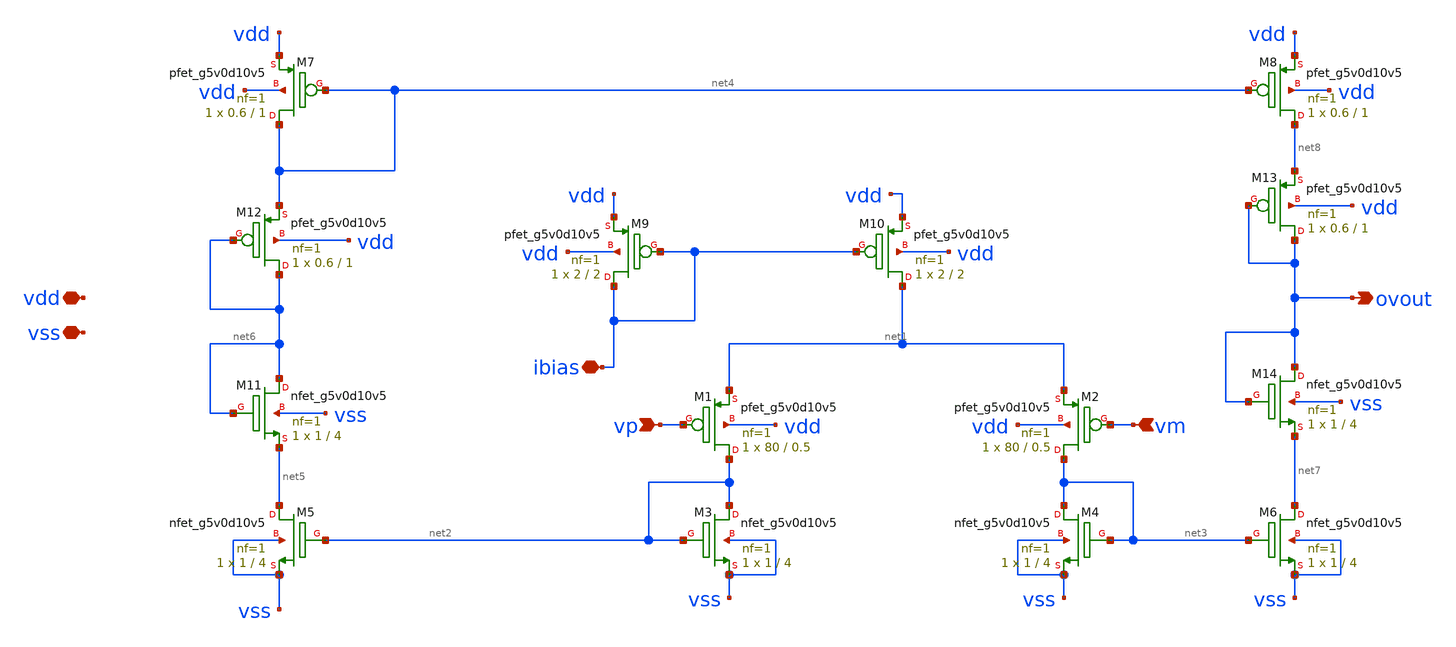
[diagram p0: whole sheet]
** sch_path: xschem/OTA.sch
**.subckt OTA ibias vdd vss vp vm ovout
*.iopin ibias
*.iopin vdd
*.iopin vss
*.ipin vp
*.ipin vm
*.opin ovout
XM1 net2 vp net1 vdd sky130_fd_pr__pfet_g5v0d10v5 L=0.5 W=80 nf=1 ad='int((nf+1)/2) * W/nf * 0.29' as='int((nf+2)/2) * W/nf * 0.29'
+ pd='2*int((nf+1)/2) * (W/nf + 0.29)' ps='2*int((nf+2)/2) * (W/nf + 0.29)' nrd='0.29 / W' nrs='0.29 / W'
+ sa=0 sb=0 sd=0 mult=1 m=1
XM2 net3 vm net1 vdd sky130_fd_pr__pfet_g5v0d10v5 L=0.5 W=80 nf=1 ad='int((nf+1)/2) * W/nf * 0.29' as='int((nf+2)/2) * W/nf * 0.29'
+ pd='2*int((nf+1)/2) * (W/nf + 0.29)' ps='2*int((nf+2)/2) * (W/nf + 0.29)' nrd='0.29 / W' nrs='0.29 / W'
+ sa=0 sb=0 sd=0 mult=1 m=1
XM3 net2 net2 vss vss sky130_fd_pr__nfet_g5v0d10v5 L=4 W=1 nf=1 ad='int((nf+1)/2) * W/nf * 0.29' as='int((nf+2)/2) * W/nf * 0.29'
+ pd='2*int((nf+1)/2) * (W/nf + 0.29)' ps='2*int((nf+2)/2) * (W/nf + 0.29)' nrd='0.29 / W' nrs='0.29 / W'
+ sa=0 sb=0 sd=0 mult=1 m=1
XM4 net3 net3 vss vss sky130_fd_pr__nfet_g5v0d10v5 L=4 W=1 nf=1 ad='int((nf+1)/2) * W/nf * 0.29' as='int((nf+2)/2) * W/nf * 0.29'
+ pd='2*int((nf+1)/2) * (W/nf + 0.29)' ps='2*int((nf+2)/2) * (W/nf + 0.29)' nrd='0.29 / W' nrs='0.29 / W'
+ sa=0 sb=0 sd=0 mult=1 m=1
XM5 net5 net2 vss vss sky130_fd_pr__nfet_g5v0d10v5 L=4 W=1 nf=1 ad='int((nf+1)/2) * W/nf * 0.29' as='int((nf+2)/2) * W/nf * 0.29'
+ pd='2*int((nf+1)/2) * (W/nf + 0.29)' ps='2*int((nf+2)/2) * (W/nf + 0.29)' nrd='0.29 / W' nrs='0.29 / W'
+ sa=0 sb=0 sd=0 mult=1 m=1
XM6 net7 net3 vss vss sky130_fd_pr__nfet_g5v0d10v5 L=4 W=1 nf=1 ad='int((nf+1)/2) * W/nf * 0.29' as='int((nf+2)/2) * W/nf * 0.29'
+ pd='2*int((nf+1)/2) * (W/nf + 0.29)' ps='2*int((nf+2)/2) * (W/nf + 0.29)' nrd='0.29 / W' nrs='0.29 / W'
+ sa=0 sb=0 sd=0 mult=1 m=1
XM7 net4 net4 vdd vdd sky130_fd_pr__pfet_g5v0d10v5 L=1 W=0.6 nf=1 ad='int((nf+1)/2) * W/nf * 0.29' as='int((nf+2)/2) * W/nf * 0.29'
+ pd='2*int((nf+1)/2) * (W/nf + 0.29)' ps='2*int((nf+2)/2) * (W/nf + 0.29)' nrd='0.29 / W' nrs='0.29 / W'
+ sa=0 sb=0 sd=0 mult=1 m=1
XM8 net8 net4 vdd vdd sky130_fd_pr__pfet_g5v0d10v5 L=1 W=0.6 nf=1 ad='int((nf+1)/2) * W/nf * 0.29' as='int((nf+2)/2) * W/nf * 0.29'
+ pd='2*int((nf+1)/2) * (W/nf + 0.29)' ps='2*int((nf+2)/2) * (W/nf + 0.29)' nrd='0.29 / W' nrs='0.29 / W'
+ sa=0 sb=0 sd=0 mult=1 m=1
XM9 ibias ibias vdd vdd sky130_fd_pr__pfet_g5v0d10v5 L=2 W=2 nf=1 ad='int((nf+1)/2) * W/nf * 0.29' as='int((nf+2)/2) * W/nf * 0.29'
+ pd='2*int((nf+1)/2) * (W/nf + 0.29)' ps='2*int((nf+2)/2) * (W/nf + 0.29)' nrd='0.29 / W' nrs='0.29 / W'
+ sa=0 sb=0 sd=0 mult=1 m=1
XM10 net1 ibias vdd vdd sky130_fd_pr__pfet_g5v0d10v5 L=2 W=2 nf=1 ad='int((nf+1)/2) * W/nf * 0.29' as='int((nf+2)/2) * W/nf * 0.29'
+ pd='2*int((nf+1)/2) * (W/nf + 0.29)' ps='2*int((nf+2)/2) * (W/nf + 0.29)' nrd='0.29 / W' nrs='0.29 / W'
+ sa=0 sb=0 sd=0 mult=1 m=1
XM11 net6 net6 net5 vss sky130_fd_pr__nfet_g5v0d10v5 L=4 W=1 nf=1 ad='int((nf+1)/2) * W/nf * 0.29' as='int((nf+2)/2) * W/nf * 0.29'
+ pd='2*int((nf+1)/2) * (W/nf + 0.29)' ps='2*int((nf+2)/2) * (W/nf + 0.29)' nrd='0.29 / W' nrs='0.29 / W'
+ sa=0 sb=0 sd=0 mult=1 m=1
XM12 net6 net6 net4 vdd sky130_fd_pr__pfet_g5v0d10v5 L=1 W=0.6 nf=1 ad='int((nf+1)/2) * W/nf * 0.29'
+ as='int((nf+2)/2) * W/nf * 0.29' pd='2*int((nf+1)/2) * (W/nf + 0.29)' ps='2*int((nf+2)/2) * (W/nf + 0.29)'
+ nrd='0.29 / W' nrs='0.29 / W' sa=0 sb=0 sd=0 mult=1 m=1
XM13 ovout ovout net8 vdd sky130_fd_pr__pfet_g5v0d10v5 L=1 W=0.6 nf=1 ad='int((nf+1)/2) * W/nf * 0.29'
+ as='int((nf+2)/2) * W/nf * 0.29' pd='2*int((nf+1)/2) * (W/nf + 0.29)' ps='2*int((nf+2)/2) * (W/nf + 0.29)'
+ nrd='0.29 / W' nrs='0.29 / W' sa=0 sb=0 sd=0 mult=1 m=1
XM14 ovout ovout net7 vss sky130_fd_pr__nfet_g5v0d10v5 L=4 W=1 nf=1 ad='int((nf+1)/2) * W/nf * 0.29'
+ as='int((nf+2)/2) * W/nf * 0.29' pd='2*int((nf+1)/2) * (W/nf + 0.29)' ps='2*int((nf+2)/2) * (W/nf + 0.29)'
+ nrd='0.29 / W' nrs='0.29 / W' sa=0 sb=0 sd=0 mult=1 m=1
**.ends
.end
